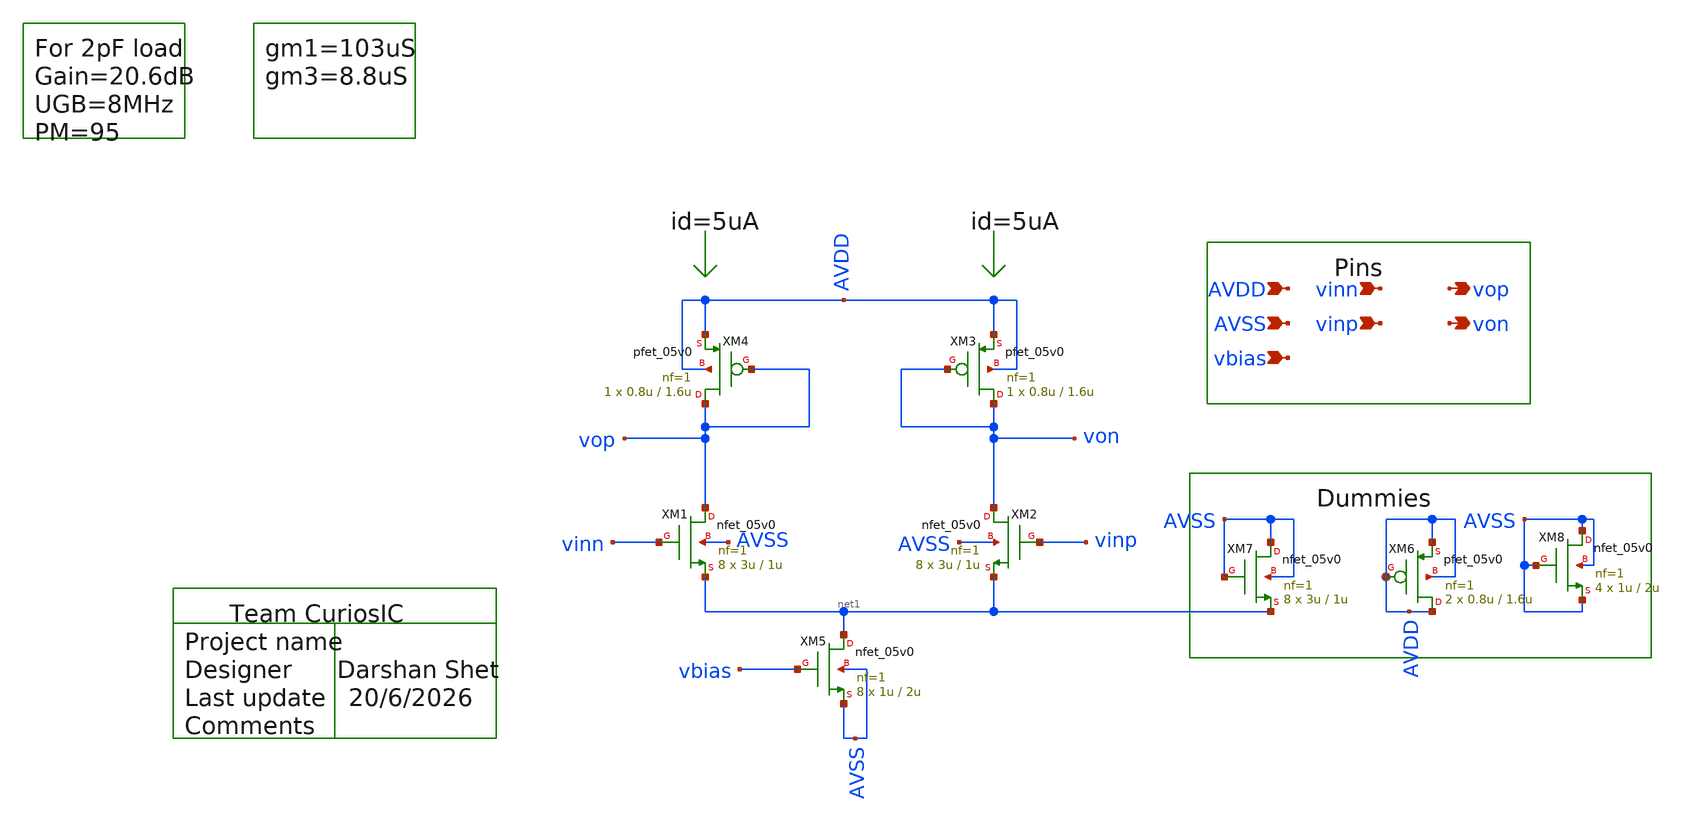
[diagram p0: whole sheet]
** sch_path: design/schematics/CCIA/Instrumentation Amplifier/DS_cic_bms_CMFB.sch
**.subckt DS_cic_bms_CMFB AVDD AVSS vinn vinp vbias vop von
*.ipin AVDD
*.ipin AVSS
*.ipin vinn
*.ipin vinp
*.ipin vbias
*.opin vop
*.opin von
XM1 vop vinn net1 AVSS nfet_05v0 L=1u W=3u nf=1 ad='int((nf+1)/2) * W/nf * 0.18u' as='int((nf+2)/2) * W/nf * 0.18u'
+ pd='2*int((nf+1)/2) * (W/nf + 0.18u)' ps='2*int((nf+2)/2) * (W/nf + 0.18u)' nrd='0.18u / W' nrs='0.18u / W'
+ sa=0 sb=0 sd=0 m=8
XM2 von vinp net1 AVSS nfet_05v0 L=1u W=3u nf=1 ad='int((nf+1)/2) * W/nf * 0.18u' as='int((nf+2)/2) * W/nf * 0.18u'
+ pd='2*int((nf+1)/2) * (W/nf + 0.18u)' ps='2*int((nf+2)/2) * (W/nf + 0.18u)' nrd='0.18u / W' nrs='0.18u / W'
+ sa=0 sb=0 sd=0 m=8
XM3 von von AVDD AVDD pfet_05v0 L=1.6u W=0.8u nf=1 ad='int((nf+1)/2) * W/nf * 0.18u' as='int((nf+2)/2) * W/nf * 0.18u'
+ pd='2*int((nf+1)/2) * (W/nf + 0.18u)' ps='2*int((nf+2)/2) * (W/nf + 0.18u)' nrd='0.18u / W' nrs='0.18u / W'
+ sa=0 sb=0 sd=0 m=1
XM4 vop vop AVDD AVDD pfet_05v0 L=1.6u W=0.8u nf=1 ad='int((nf+1)/2) * W/nf * 0.18u' as='int((nf+2)/2) * W/nf * 0.18u'
+ pd='2*int((nf+1)/2) * (W/nf + 0.18u)' ps='2*int((nf+2)/2) * (W/nf + 0.18u)' nrd='0.18u / W' nrs='0.18u / W'
+ sa=0 sb=0 sd=0 m=1
XM5 net1 vbias AVSS AVSS nfet_05v0 L=2u W=1u nf=1 ad='int((nf+1)/2) * W/nf * 0.18u' as='int((nf+2)/2) * W/nf * 0.18u'
+ pd='2*int((nf+1)/2) * (W/nf + 0.18u)' ps='2*int((nf+2)/2) * (W/nf + 0.18u)' nrd='0.18u / W' nrs='0.18u / W'
+ sa=0 sb=0 sd=0 m=8
XM6 AVDD AVDD AVDD AVDD pfet_05v0 L=1.6u W=0.8u nf=1 ad='int((nf+1)/2) * W/nf * 0.18u' as='int((nf+2)/2) * W/nf * 0.18u'
+ pd='2*int((nf+1)/2) * (W/nf + 0.18u)' ps='2*int((nf+2)/2) * (W/nf + 0.18u)' nrd='0.18u / W' nrs='0.18u / W'
+ sa=0 sb=0 sd=0 m=2
XM7 AVSS AVSS net1 AVSS nfet_05v0 L=1u W=3u nf=1 ad='int((nf+1)/2) * W/nf * 0.18u' as='int((nf+2)/2) * W/nf * 0.18u'
+ pd='2*int((nf+1)/2) * (W/nf + 0.18u)' ps='2*int((nf+2)/2) * (W/nf + 0.18u)' nrd='0.18u / W' nrs='0.18u / W'
+ sa=0 sb=0 sd=0 m=8
XM8 AVSS AVSS AVSS AVSS nfet_05v0 L=2u W=1u nf=1 ad='int((nf+1)/2) * W/nf * 0.18u' as='int((nf+2)/2) * W/nf * 0.18u'
+ pd='2*int((nf+1)/2) * (W/nf + 0.18u)' ps='2*int((nf+2)/2) * (W/nf + 0.18u)' nrd='0.18u / W' nrs='0.18u / W'
+ sa=0 sb=0 sd=0 m=4
**.ends
.end
